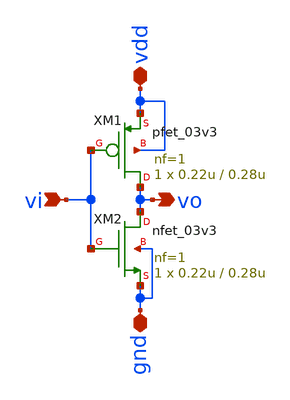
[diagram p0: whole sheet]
** sch_path: inverter.sch
**.subckt inverter vi vo vdd gnd
*.ipin vi
*.opin vo
*.iopin vdd
*.iopin gnd
XM1 vo vi vdd vdd pfet_03v3 L=0.28u W=0.22u nf=1 ad='int((nf+1)/2) * W/nf * 0.18u' as='int((nf+2)/2) * W/nf * 0.18u'
+ pd='2*int((nf+1)/2) * (W/nf + 0.18u)' ps='2*int((nf+2)/2) * (W/nf + 0.18u)' nrd='0.18u / W' nrs='0.18u / W'
+ sa=0 sb=0 sd=0 m=1
XM2 vo vi gnd gnd nfet_03v3 L=0.28u W=0.22u nf=1 ad='int((nf+1)/2) * W/nf * 0.18u' as='int((nf+2)/2) * W/nf * 0.18u'
+ pd='2*int((nf+1)/2) * (W/nf + 0.18u)' ps='2*int((nf+2)/2) * (W/nf + 0.18u)' nrd='0.18u / W' nrs='0.18u / W'
+ sa=0 sb=0 sd=0 m=1
**.ends
.end
